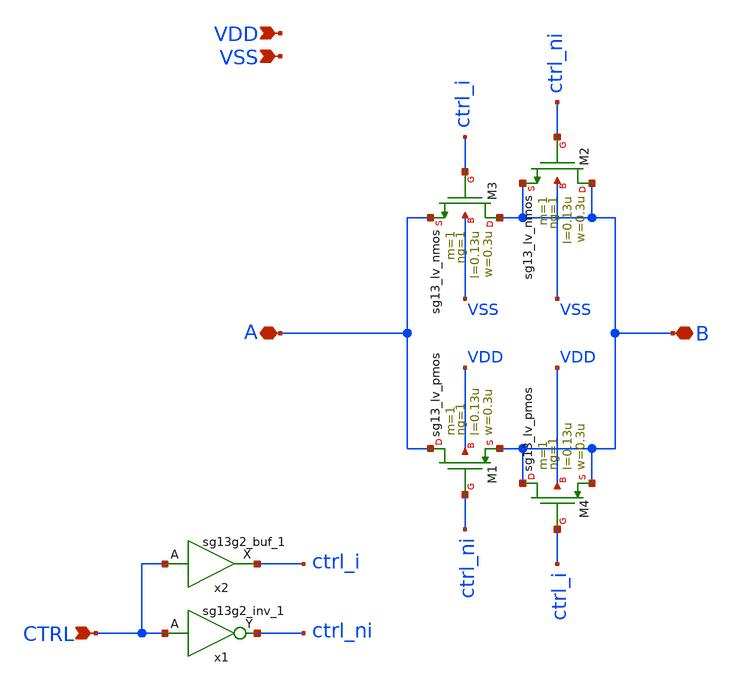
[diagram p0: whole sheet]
** sch_path: designs/tgate/tgate.sch
* IHP-GmbH/IHP-Open-PDK/ihp-sg13g2/libs.tech/xschem/sg13g2_stdcells/sg13g2_buf_1.sch:
* Copyright 2023 IHP PDK Authors
* Licensed under the Apache License, Version 2.0 (the "License");
**.subckt tgate CTRL B A VDD VSS
*.ipin CTRL
*.iopin B
*.iopin A
*.ipin VDD
*.ipin VSS
x1 ctrl_ni CTRL VDD VSS sg13g2_inv_1
XM3 B ctrl_i A VSS sg13_lv_nmos w=0.3u l=0.13u ng=1 m=1 mm_ok=1
XM1 A ctrl_ni B VDD sg13_lv_pmos w=0.3u l=0.13u ng=1 m=1 mm_ok=1
x2 ctrl_i CTRL VDD VSS sg13g2_buf_1
XM2 B ctrl_ni B VSS sg13_lv_nmos w=0.3u l=0.13u ng=1 m=1 mm_ok=1
XM4 B ctrl_i B VDD sg13_lv_pmos w=0.3u l=0.13u ng=1 m=1 mm_ok=1
**.ends

* expanding   symbol:  sg13g2_stdcells/sg13g2_inv_1.sym # of pins=2
** sym_path: sg13g2_stdcells/sg13g2_inv_1.sym
** sch_path: sg13g2_stdcells/sg13g2_inv_1.sch
.subckt sg13g2_inv_1 Y A VDD VSS
*.opin Y
*.ipin A
*.iopin VDD
*.iopin VSS
XM1 Y A VSS VSS sg13_lv_nmos w=740.00n l=130.00n ng=1 m=1 mm_ok=1
XM2 Y A VDD VDD sg13_lv_pmos w=1.12u l=130.00n ng=1 m=1 mm_ok=1
.ends


* expanding   symbol:  sg13g2_stdcells/sg13g2_buf_1.sym # of pins=2
** sym_path: sg13g2_stdcells/sg13g2_buf_1.sym
** sch_path: sg13g2_stdcells/sg13g2_buf_1.sch
.subckt sg13g2_buf_1 X A VDD VSS
*.ipin A
*.opin X
*.iopin VDD
*.iopin VSS
XM1 net1 A VSS VSS sg13_lv_nmos w=550.00n l=130.00n ng=1 m=1 mm_ok=1
XM2 X net1 VSS VSS sg13_lv_nmos w=740.00n l=130.00n ng=1 m=1 mm_ok=1
XM3 net1 A VDD VDD sg13_lv_pmos w=840.00n l=130.00n ng=1 m=1 mm_ok=1
XM4 X net1 VDD VDD sg13_lv_pmos w=1.12u l=130.00n ng=1 m=1 mm_ok=1
.ends

.end
